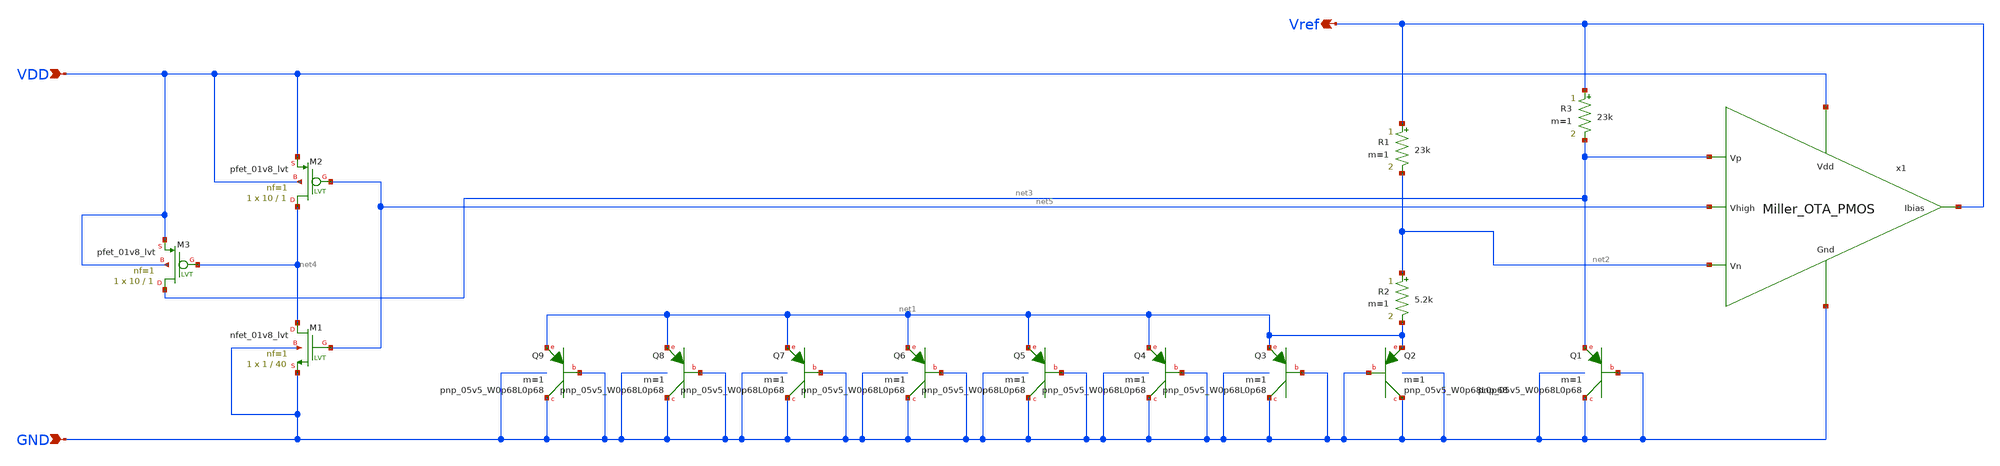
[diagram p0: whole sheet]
** sch_path: Bandgap/Schematics/BGR1.8v/Bandgap1.8v.sch
**.subckt Bandgap1.8v VDD GND Vref
*.ipin VDD
*.ipin GND
*.opin Vref
R1 Vref net2 23k m=1
R2 net2 net1 5.2k m=1
R3 Vref net3 23k m=1
XQ1 GND GND net3 sky130_fd_pr__pnp_05v5_W0p68L0p68 m=1
XQ2 GND GND net1 sky130_fd_pr__pnp_05v5_W0p68L0p68 m=1
XQ3 GND GND net1 sky130_fd_pr__pnp_05v5_W0p68L0p68 m=1
XQ4 GND GND net1 sky130_fd_pr__pnp_05v5_W0p68L0p68 m=1
XQ5 GND GND net1 sky130_fd_pr__pnp_05v5_W0p68L0p68 m=1
XQ6 GND GND net1 sky130_fd_pr__pnp_05v5_W0p68L0p68 m=1
XQ7 GND GND net1 sky130_fd_pr__pnp_05v5_W0p68L0p68 m=1
XQ8 GND GND net1 sky130_fd_pr__pnp_05v5_W0p68L0p68 m=1
XQ9 GND GND net1 sky130_fd_pr__pnp_05v5_W0p68L0p68 m=1
x1 VDD net3 net2 Vref net5 GND Miller_OTA_PMOS
XM1 net4 net5 GND GND sky130_fd_pr__nfet_01v8_lvt L=40 W=1 nf=1 ad='int((nf+1)/2) * W/nf * 0.29' as='int((nf+2)/2) * W/nf * 0.29'
+ pd='2*int((nf+1)/2) * (W/nf + 0.29)' ps='2*int((nf+2)/2) * (W/nf + 0.29)' nrd='0.29 / W' nrs='0.29 / W'
+ sa=0 sb=0 sd=0 mult=1 m=1
XM2 net4 net5 VDD VDD sky130_fd_pr__pfet_01v8_lvt L=1 W=10 nf=1 ad='int((nf+1)/2) * W/nf * 0.29' as='int((nf+2)/2) * W/nf * 0.29'
+ pd='2*int((nf+1)/2) * (W/nf + 0.29)' ps='2*int((nf+2)/2) * (W/nf + 0.29)' nrd='0.29 / W' nrs='0.29 / W'
+ sa=0 sb=0 sd=0 mult=1 m=1
XM3 net3 net4 VDD VDD sky130_fd_pr__pfet_01v8_lvt L=1 W=10 nf=1 ad='int((nf+1)/2) * W/nf * 0.29' as='int((nf+2)/2) * W/nf * 0.29'
+ pd='2*int((nf+1)/2) * (W/nf + 0.29)' ps='2*int((nf+2)/2) * (W/nf + 0.29)' nrd='0.29 / W' nrs='0.29 / W'
+ sa=0 sb=0 sd=0 mult=1 m=1
**.ends

* expanding   symbol:  /home/eslam/Analog_Design/OTA/Schematic/Miller_OTA_PMOS.sym # of pins=6
** sym_path: OTA/Schematic/Miller_OTA_PMOS.sym
** sch_path: OTA/Schematic/Miller_OTA_PMOS.sch
.subckt Miller_OTA_PMOS Vdd Vp Vn Ibias Vhigh Gnd
*.ipin Vp
*.ipin Vn
*.opin Ibias
*.ipin Vdd
*.ipin Gnd
*.ipin Vhigh
XM6 Ibias Vhigh Vdd Vdd sky130_fd_pr__pfet_g5v0d10v5 L=1 W=10 nf=1 ad='int((nf+1)/2) * W/nf * 0.29' as='int((nf+2)/2) * W/nf * 0.29'
+ pd='2*int((nf+1)/2) * (W/nf + 0.29)' ps='2*int((nf+2)/2) * (W/nf + 0.29)' nrd='0.29 / W' nrs='0.29 / W'
+ sa=0 sb=0 sd=0 mult=1 m=1
XM5 net3 Vhigh Vdd Vdd sky130_fd_pr__pfet_g5v0d10v5 L=1 W=10 nf=1 ad='int((nf+1)/2) * W/nf * 0.29' as='int((nf+2)/2) * W/nf * 0.29'
+ pd='2*int((nf+1)/2) * (W/nf + 0.29)' ps='2*int((nf+2)/2) * (W/nf + 0.29)' nrd='0.29 / W' nrs='0.29 / W'
+ sa=0 sb=0 sd=0 mult=1 m=1
XM7 Vhigh Vhigh Vdd Vdd sky130_fd_pr__pfet_g5v0d10v5 L=1 W=54 nf=1 ad='int((nf+1)/2) * W/nf * 0.29' as='int((nf+2)/2) * W/nf * 0.29'
+ pd='2*int((nf+1)/2) * (W/nf + 0.29)' ps='2*int((nf+2)/2) * (W/nf + 0.29)' nrd='0.29 / W' nrs='0.29 / W'
+ sa=0 sb=0 sd=0 mult=1 m=1
XC1 net1 Vhigh sky130_fd_pr__cap_mim_m3_2 W=1 L=1 MF=1 m=1
XM1 net2 Vn net3 Vdd sky130_fd_pr__pfet_g5v0d10v5 L=1 W=30 nf=1 ad='int((nf+1)/2) * W/nf * 0.29' as='int((nf+2)/2) * W/nf * 0.29'
+ pd='2*int((nf+1)/2) * (W/nf + 0.29)' ps='2*int((nf+2)/2) * (W/nf + 0.29)' nrd='0.29 / W' nrs='0.29 / W'
+ sa=0 sb=0 sd=0 mult=1 m=1
XM2 net1 Vp net3 Vdd sky130_fd_pr__pfet_g5v0d10v5 L=1 W=30 nf=1 ad='int((nf+1)/2) * W/nf * 0.29' as='int((nf+2)/2) * W/nf * 0.29'
+ pd='2*int((nf+1)/2) * (W/nf + 0.29)' ps='2*int((nf+2)/2) * (W/nf + 0.29)' nrd='0.29 / W' nrs='0.29 / W'
+ sa=0 sb=0 sd=0 mult=1 m=1
XM8 Vhigh net1 Gnd Gnd sky130_fd_pr__nfet_g5v0d10v5 L=0.5 W=75 nf=1 ad='int((nf+1)/2) * W/nf * 0.29'
+ as='int((nf+2)/2) * W/nf * 0.29' pd='2*int((nf+1)/2) * (W/nf + 0.29)' ps='2*int((nf+2)/2) * (W/nf + 0.29)'
+ nrd='0.29 / W' nrs='0.29 / W' sa=0 sb=0 sd=0 mult=1 m=1
XM4 net1 net2 Gnd Gnd sky130_fd_pr__nfet_g5v0d10v5 L=0.5 W=7.4 nf=1 ad='int((nf+1)/2) * W/nf * 0.29'
+ as='int((nf+2)/2) * W/nf * 0.29' pd='2*int((nf+1)/2) * (W/nf + 0.29)' ps='2*int((nf+2)/2) * (W/nf + 0.29)'
+ nrd='0.29 / W' nrs='0.29 / W' sa=0 sb=0 sd=0 mult=1 m=1
XM3 net2 net2 Gnd Gnd sky130_fd_pr__nfet_g5v0d10v5 L=0.5 W=7.4 nf=1 ad='int((nf+1)/2) * W/nf * 0.29'
+ as='int((nf+2)/2) * W/nf * 0.29' pd='2*int((nf+1)/2) * (W/nf + 0.29)' ps='2*int((nf+2)/2) * (W/nf + 0.29)'
+ nrd='0.29 / W' nrs='0.29 / W' sa=0 sb=0 sd=0 mult=1 m=1
.ends

.end
